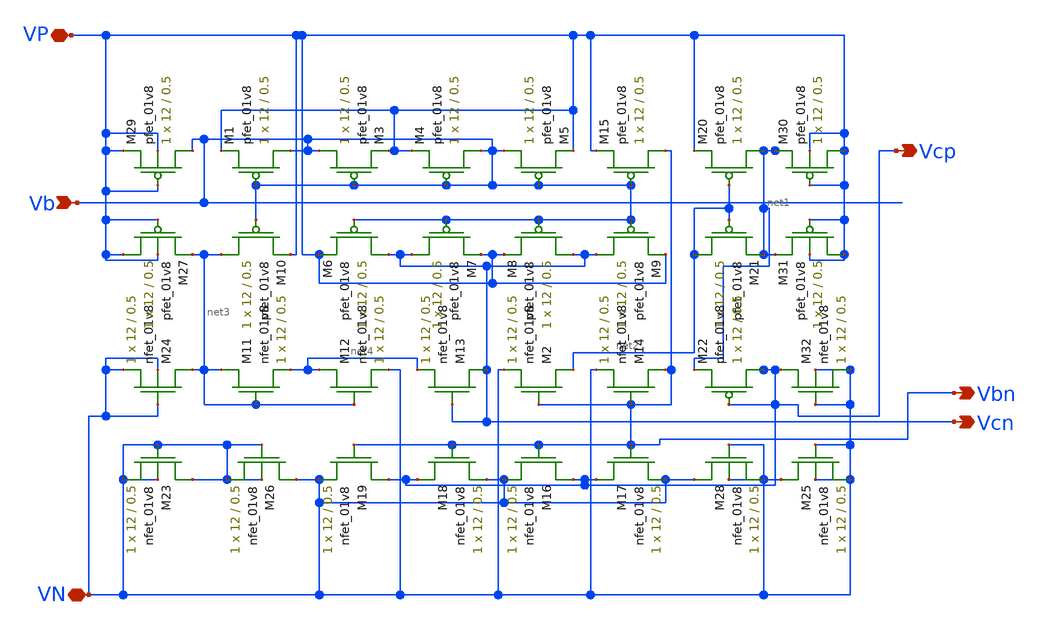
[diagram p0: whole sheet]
** sch_path: MiniProject3-Cascode/XSCHEM/VoltageGenerator.sch
**.subckt VoltageGenerator VP VN Vcn Vcp Vbn Vb
*.iopin VP
*.iopin VN
*.opin Vcn
*.opin Vcp
*.opin Vbn
*.ipin Vb
XM1 Vb Vb VP VDD sky130_fd_pr__pfet_01v8 L=0.5 W=12 nf=1 ad='int((nf+1)/2) * W/nf * 0.29' as='int((nf+2)/2) * W/nf * 0.29'
+ pd='2*int((nf+1)/2) * (W/nf + 0.29)' ps='2*int((nf+2)/2) * (W/nf + 0.29)' nrd='0.29 / W' nrs='0.29 / W'
+ sa=0 sb=0 sd=0 mult=1 m=1
XM2 net2 Vbn VN GND sky130_fd_pr__nfet_01v8 L=0.5 W=12 nf=1 ad='int((nf+1)/2) * W/nf * 0.29' as='int((nf+2)/2) * W/nf * 0.29'
+ pd='2*int((nf+1)/2) * (W/nf + 0.29)' ps='2*int((nf+2)/2) * (W/nf + 0.29)' nrd='0.29 / W' nrs='0.29 / W'
+ sa=0 sb=0 sd=0 mult=1 m=1
XM3 Vb Vb VP VDD sky130_fd_pr__pfet_01v8 L=0.5 W=12 nf=1 ad='int((nf+1)/2) * W/nf * 0.29' as='int((nf+2)/2) * W/nf * 0.29'
+ pd='2*int((nf+1)/2) * (W/nf + 0.29)' ps='2*int((nf+2)/2) * (W/nf + 0.29)' nrd='0.29 / W' nrs='0.29 / W'
+ sa=0 sb=0 sd=0 mult=1 m=1
XM4 Vb Vb VP VDD sky130_fd_pr__pfet_01v8 L=0.5 W=12 nf=1 ad='int((nf+1)/2) * W/nf * 0.29' as='int((nf+2)/2) * W/nf * 0.29'
+ pd='2*int((nf+1)/2) * (W/nf + 0.29)' ps='2*int((nf+2)/2) * (W/nf + 0.29)' nrd='0.29 / W' nrs='0.29 / W'
+ sa=0 sb=0 sd=0 mult=1 m=1
XM5 Vb Vb VP VDD sky130_fd_pr__pfet_01v8 L=0.5 W=12 nf=1 ad='int((nf+1)/2) * W/nf * 0.29' as='int((nf+2)/2) * W/nf * 0.29'
+ pd='2*int((nf+1)/2) * (W/nf + 0.29)' ps='2*int((nf+2)/2) * (W/nf + 0.29)' nrd='0.29 / W' nrs='0.29 / W'
+ sa=0 sb=0 sd=0 mult=1 m=1
XM6 Vcn Vb VP VDD sky130_fd_pr__pfet_01v8 L=0.5 W=12 nf=1 ad='int((nf+1)/2) * W/nf * 0.29' as='int((nf+2)/2) * W/nf * 0.29'
+ pd='2*int((nf+1)/2) * (W/nf + 0.29)' ps='2*int((nf+2)/2) * (W/nf + 0.29)' nrd='0.29 / W' nrs='0.29 / W'
+ sa=0 sb=0 sd=0 mult=1 m=1
XM7 Vcn Vb VP VDD sky130_fd_pr__pfet_01v8 L=0.5 W=12 nf=1 ad='int((nf+1)/2) * W/nf * 0.29' as='int((nf+2)/2) * W/nf * 0.29'
+ pd='2*int((nf+1)/2) * (W/nf + 0.29)' ps='2*int((nf+2)/2) * (W/nf + 0.29)' nrd='0.29 / W' nrs='0.29 / W'
+ sa=0 sb=0 sd=0 mult=1 m=1
XM8 Vcn Vb VP VDD sky130_fd_pr__pfet_01v8 L=0.5 W=12 nf=1 ad='int((nf+1)/2) * W/nf * 0.29' as='int((nf+2)/2) * W/nf * 0.29'
+ pd='2*int((nf+1)/2) * (W/nf + 0.29)' ps='2*int((nf+2)/2) * (W/nf + 0.29)' nrd='0.29 / W' nrs='0.29 / W'
+ sa=0 sb=0 sd=0 mult=1 m=1
XM9 Vcn Vb VP VDD sky130_fd_pr__pfet_01v8 L=0.5 W=12 nf=1 ad='int((nf+1)/2) * W/nf * 0.29' as='int((nf+2)/2) * W/nf * 0.29'
+ pd='2*int((nf+1)/2) * (W/nf + 0.29)' ps='2*int((nf+2)/2) * (W/nf + 0.29)' nrd='0.29 / W' nrs='0.29 / W'
+ sa=0 sb=0 sd=0 mult=1 m=1
XM10 net3 Vb VP VDD sky130_fd_pr__pfet_01v8 L=0.5 W=12 nf=1 ad='int((nf+1)/2) * W/nf * 0.29' as='int((nf+2)/2) * W/nf * 0.29'
+ pd='2*int((nf+1)/2) * (W/nf + 0.29)' ps='2*int((nf+2)/2) * (W/nf + 0.29)' nrd='0.29 / W' nrs='0.29 / W'
+ sa=0 sb=0 sd=0 mult=1 m=1
XM11 net3 net3 net4 GND sky130_fd_pr__nfet_01v8 L=0.5 W=12 nf=1 ad='int((nf+1)/2) * W/nf * 0.29' as='int((nf+2)/2) * W/nf * 0.29'
+ pd='2*int((nf+1)/2) * (W/nf + 0.29)' ps='2*int((nf+2)/2) * (W/nf + 0.29)' nrd='0.29 / W' nrs='0.29 / W'
+ sa=0 sb=0 sd=0 mult=1 m=1
XM12 net4 net3 VN GND sky130_fd_pr__nfet_01v8 L=0.5 W=12 nf=1 ad='int((nf+1)/2) * W/nf * 0.29' as='int((nf+2)/2) * W/nf * 0.29'
+ pd='2*int((nf+1)/2) * (W/nf + 0.29)' ps='2*int((nf+2)/2) * (W/nf + 0.29)' nrd='0.29 / W' nrs='0.29 / W'
+ sa=0 sb=0 sd=0 mult=1 m=1
XM13 Vcn Vcn net4 GND sky130_fd_pr__nfet_01v8 L=0.5 W=12 nf=1 ad='int((nf+1)/2) * W/nf * 0.29' as='int((nf+2)/2) * W/nf * 0.29'
+ pd='2*int((nf+1)/2) * (W/nf + 0.29)' ps='2*int((nf+2)/2) * (W/nf + 0.29)' nrd='0.29 / W' nrs='0.29 / W'
+ sa=0 sb=0 sd=0 mult=1 m=1
XM14 Vbn Vbn VN GND sky130_fd_pr__nfet_01v8 L=0.5 W=12 nf=1 ad='int((nf+1)/2) * W/nf * 0.29' as='int((nf+2)/2) * W/nf * 0.29'
+ pd='2*int((nf+1)/2) * (W/nf + 0.29)' ps='2*int((nf+2)/2) * (W/nf + 0.29)' nrd='0.29 / W' nrs='0.29 / W'
+ sa=0 sb=0 sd=0 mult=1 m=1
XM15 Vbn Vb VP VDD sky130_fd_pr__pfet_01v8 L=0.5 W=12 nf=1 ad='int((nf+1)/2) * W/nf * 0.29' as='int((nf+2)/2) * W/nf * 0.29'
+ pd='2*int((nf+1)/2) * (W/nf + 0.29)' ps='2*int((nf+2)/2) * (W/nf + 0.29)' nrd='0.29 / W' nrs='0.29 / W'
+ sa=0 sb=0 sd=0 mult=1 m=1
XM16 Vcp Vbn VN GND sky130_fd_pr__nfet_01v8 L=0.5 W=12 nf=1 ad='int((nf+1)/2) * W/nf * 0.29' as='int((nf+2)/2) * W/nf * 0.29'
+ pd='2*int((nf+1)/2) * (W/nf + 0.29)' ps='2*int((nf+2)/2) * (W/nf + 0.29)' nrd='0.29 / W' nrs='0.29 / W'
+ sa=0 sb=0 sd=0 mult=1 m=1
XM17 Vcp Vbn VN GND sky130_fd_pr__nfet_01v8 L=0.5 W=12 nf=1 ad='int((nf+1)/2) * W/nf * 0.29' as='int((nf+2)/2) * W/nf * 0.29'
+ pd='2*int((nf+1)/2) * (W/nf + 0.29)' ps='2*int((nf+2)/2) * (W/nf + 0.29)' nrd='0.29 / W' nrs='0.29 / W'
+ sa=0 sb=0 sd=0 mult=1 m=1
XM18 Vcp Vbn VN GND sky130_fd_pr__nfet_01v8 L=0.5 W=12 nf=1 ad='int((nf+1)/2) * W/nf * 0.29' as='int((nf+2)/2) * W/nf * 0.29'
+ pd='2*int((nf+1)/2) * (W/nf + 0.29)' ps='2*int((nf+2)/2) * (W/nf + 0.29)' nrd='0.29 / W' nrs='0.29 / W'
+ sa=0 sb=0 sd=0 mult=1 m=1
XM19 Vcp Vbn VN GND sky130_fd_pr__nfet_01v8 L=0.5 W=12 nf=1 ad='int((nf+1)/2) * W/nf * 0.29' as='int((nf+2)/2) * W/nf * 0.29'
+ pd='2*int((nf+1)/2) * (W/nf + 0.29)' ps='2*int((nf+2)/2) * (W/nf + 0.29)' nrd='0.29 / W' nrs='0.29 / W'
+ sa=0 sb=0 sd=0 mult=1 m=1
XM20 net1 net2 VP VDD sky130_fd_pr__pfet_01v8 L=0.5 W=12 nf=1 ad='int((nf+1)/2) * W/nf * 0.29' as='int((nf+2)/2) * W/nf * 0.29'
+ pd='2*int((nf+1)/2) * (W/nf + 0.29)' ps='2*int((nf+2)/2) * (W/nf + 0.29)' nrd='0.29 / W' nrs='0.29 / W'
+ sa=0 sb=0 sd=0 mult=1 m=1
XM21 net2 net2 net1 VDD sky130_fd_pr__pfet_01v8 L=0.5 W=12 nf=1 ad='int((nf+1)/2) * W/nf * 0.29' as='int((nf+2)/2) * W/nf * 0.29'
+ pd='2*int((nf+1)/2) * (W/nf + 0.29)' ps='2*int((nf+2)/2) * (W/nf + 0.29)' nrd='0.29 / W' nrs='0.29 / W'
+ sa=0 sb=0 sd=0 mult=1 m=1
XM22 Vcp Vcp net1 VDD sky130_fd_pr__pfet_01v8 L=0.5 W=12 nf=1 ad='int((nf+1)/2) * W/nf * 0.29' as='int((nf+2)/2) * W/nf * 0.29'
+ pd='2*int((nf+1)/2) * (W/nf + 0.29)' ps='2*int((nf+2)/2) * (W/nf + 0.29)' nrd='0.29 / W' nrs='0.29 / W'
+ sa=0 sb=0 sd=0 mult=1 m=1
XM24 net3 VN VN VN sky130_fd_pr__nfet_01v8 L=0.5 W=12 nf=1 ad='int((nf+1)/2) * W/nf * 0.29' as='int((nf+2)/2) * W/nf * 0.29'
+ pd='2*int((nf+1)/2) * (W/nf + 0.29)' ps='2*int((nf+2)/2) * (W/nf + 0.29)' nrd='0.29 / W' nrs='0.29 / W'
+ sa=0 sb=0 sd=0 mult=1 m=1
XM25 VN VN VN VN sky130_fd_pr__nfet_01v8 L=0.5 W=12 nf=1 ad='int((nf+1)/2) * W/nf * 0.29' as='int((nf+2)/2) * W/nf * 0.29'
+ pd='2*int((nf+1)/2) * (W/nf + 0.29)' ps='2*int((nf+2)/2) * (W/nf + 0.29)' nrd='0.29 / W' nrs='0.29 / W'
+ sa=0 sb=0 sd=0 mult=1 m=1
XM27 VP VP net3 VP sky130_fd_pr__pfet_01v8 L=0.5 W=12 nf=1 ad='int((nf+1)/2) * W/nf * 0.29' as='int((nf+2)/2) * W/nf * 0.29'
+ pd='2*int((nf+1)/2) * (W/nf + 0.29)' ps='2*int((nf+2)/2) * (W/nf + 0.29)' nrd='0.29 / W' nrs='0.29 / W'
+ sa=0 sb=0 sd=0 mult=1 m=1
XM29 Vb VP VP VP sky130_fd_pr__pfet_01v8 L=0.5 W=12 nf=1 ad='int((nf+1)/2) * W/nf * 0.29' as='int((nf+2)/2) * W/nf * 0.29'
+ pd='2*int((nf+1)/2) * (W/nf + 0.29)' ps='2*int((nf+2)/2) * (W/nf + 0.29)' nrd='0.29 / W' nrs='0.29 / W'
+ sa=0 sb=0 sd=0 mult=1 m=1
XM30 VP VP net1 VP sky130_fd_pr__pfet_01v8 L=0.5 W=12 nf=1 ad='int((nf+1)/2) * W/nf * 0.29' as='int((nf+2)/2) * W/nf * 0.29'
+ pd='2*int((nf+1)/2) * (W/nf + 0.29)' ps='2*int((nf+2)/2) * (W/nf + 0.29)' nrd='0.29 / W' nrs='0.29 / W'
+ sa=0 sb=0 sd=0 mult=1 m=1
XM31 VP VP net1 VP sky130_fd_pr__pfet_01v8 L=0.5 W=12 nf=1 ad='int((nf+1)/2) * W/nf * 0.29' as='int((nf+2)/2) * W/nf * 0.29'
+ pd='2*int((nf+1)/2) * (W/nf + 0.29)' ps='2*int((nf+2)/2) * (W/nf + 0.29)' nrd='0.29 / W' nrs='0.29 / W'
+ sa=0 sb=0 sd=0 mult=1 m=1
XM32 Vcp VN VN VN sky130_fd_pr__nfet_01v8 L=0.5 W=12 nf=1 ad='int((nf+1)/2) * W/nf * 0.29' as='int((nf+2)/2) * W/nf * 0.29'
+ pd='2*int((nf+1)/2) * (W/nf + 0.29)' ps='2*int((nf+2)/2) * (W/nf + 0.29)' nrd='0.29 / W' nrs='0.29 / W'
+ sa=0 sb=0 sd=0 mult=1 m=1
XM28 VN VN VN VN sky130_fd_pr__nfet_01v8 L=0.5 W=12 nf=1 ad='int((nf+1)/2) * W/nf * 0.29' as='int((nf+2)/2) * W/nf * 0.29'
+ pd='2*int((nf+1)/2) * (W/nf + 0.29)' ps='2*int((nf+2)/2) * (W/nf + 0.29)' nrd='0.29 / W' nrs='0.29 / W'
+ sa=0 sb=0 sd=0 mult=1 m=1
XM26 VN VN VN VN sky130_fd_pr__nfet_01v8 L=0.5 W=12 nf=1 ad='int((nf+1)/2) * W/nf * 0.29' as='int((nf+2)/2) * W/nf * 0.29'
+ pd='2*int((nf+1)/2) * (W/nf + 0.29)' ps='2*int((nf+2)/2) * (W/nf + 0.29)' nrd='0.29 / W' nrs='0.29 / W'
+ sa=0 sb=0 sd=0 mult=1 m=1
XM23 VN VN VN VN sky130_fd_pr__nfet_01v8 L=0.5 W=12 nf=1 ad='int((nf+1)/2) * W/nf * 0.29' as='int((nf+2)/2) * W/nf * 0.29'
+ pd='2*int((nf+1)/2) * (W/nf + 0.29)' ps='2*int((nf+2)/2) * (W/nf + 0.29)' nrd='0.29 / W' nrs='0.29 / W'
+ sa=0 sb=0 sd=0 mult=1 m=1
**.ends
.end
